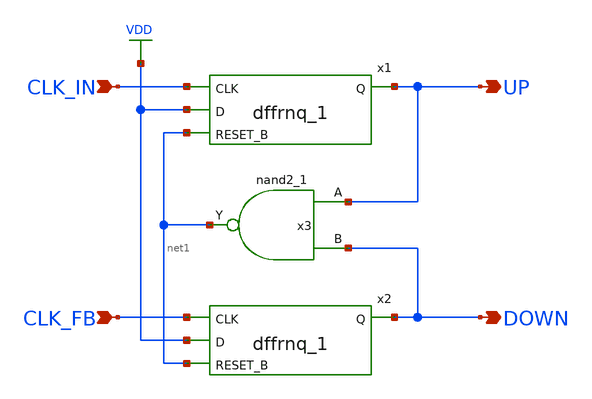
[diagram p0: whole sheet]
** sch_path: designs/libs/core_analog/pfd/pfd.sch
**.subckt pfd UP DOWN CLK_IN CLK_FB
*.opin UP
*.opin DOWN
*.ipin CLK_IN
*.ipin CLK_FB
x1 VDD net1 CLK_IN UP VDD VDD GND GND gf180mcu_fd_sc_mcu7t5v0__dffrnq_1
x2 VDD net1 CLK_FB DOWN VDD VDD GND GND gf180mcu_fd_sc_mcu7t5v0__dffrnq_1
x3 UP DOWN net1 VDD VDD GND GND gf180mcu_fd_sc_mcu7t5v0__nand2_1
**.ends
.GLOBAL VDD
.end
